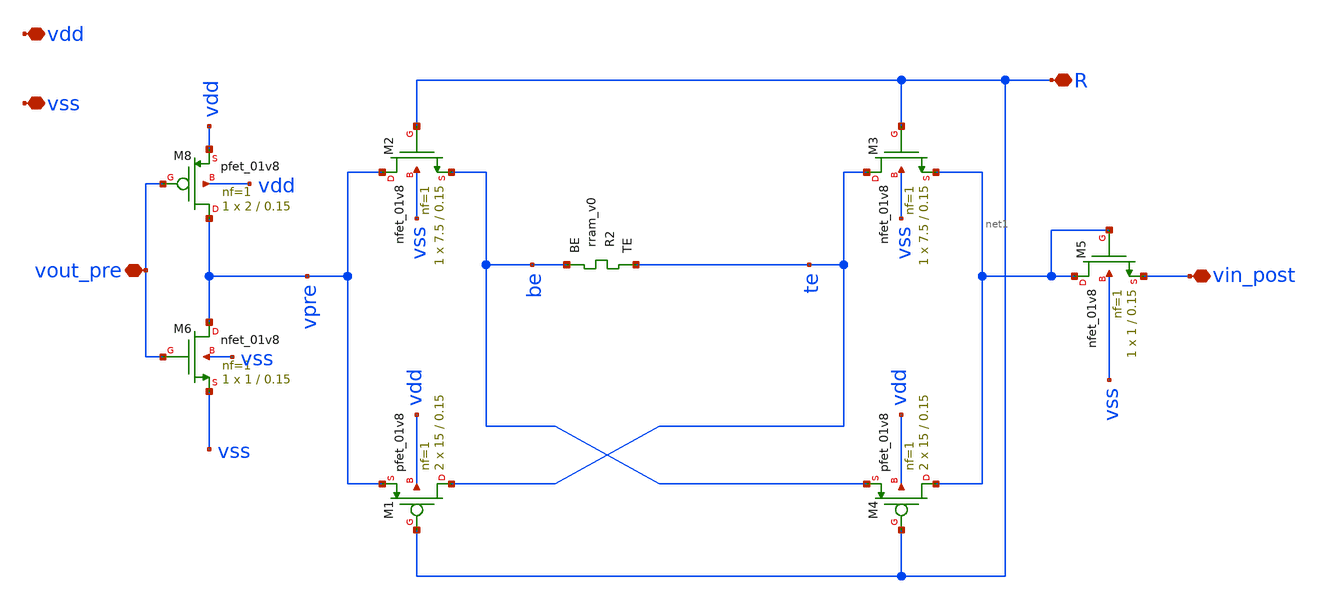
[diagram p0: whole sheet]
** sch_path: Synapse/rstdp_foward.sch
**.subckt rstdp_foward vdd vss R vin_post vout_pre
*.iopin vdd
*.iopin vss
*.iopin R
*.iopin vin_post
*.iopin vout_pre
XR2 te be rram_v0
XM2 vpre R be vss sky130_fd_pr__nfet_01v8 L=0.15 W=7.5 nf=1 ad='int((nf+1)/2) * W/nf * 0.29' as='int((nf+2)/2) * W/nf * 0.29'
+ pd='2*int((nf+1)/2) * (W/nf + 0.29)' ps='2*int((nf+2)/2) * (W/nf + 0.29)' nrd='0.29 / W' nrs='0.29 / W'
+ sa=0 sb=0 sd=0 mult=1 m=1
XM3 te R net1 vss sky130_fd_pr__nfet_01v8 L=0.15 W=7.5 nf=1 ad='int((nf+1)/2) * W/nf * 0.29' as='int((nf+2)/2) * W/nf * 0.29'
+ pd='2*int((nf+1)/2) * (W/nf + 0.29)' ps='2*int((nf+2)/2) * (W/nf + 0.29)' nrd='0.29 / W' nrs='0.29 / W'
+ sa=0 sb=0 sd=0 mult=1 m=1
XM1 te R vpre vdd sky130_fd_pr__pfet_01v8 L=0.15 W=15 nf=1 ad='int((nf+1)/2) * W/nf * 0.29' as='int((nf+2)/2) * W/nf * 0.29'
+ pd='2*int((nf+1)/2) * (W/nf + 0.29)' ps='2*int((nf+2)/2) * (W/nf + 0.29)' nrd='0.29 / W' nrs='0.29 / W'
+ sa=0 sb=0 sd=0 mult=2 m=2
XM4 net1 R be vdd sky130_fd_pr__pfet_01v8 L=0.15 W=15 nf=1 ad='int((nf+1)/2) * W/nf * 0.29' as='int((nf+2)/2) * W/nf * 0.29'
+ pd='2*int((nf+1)/2) * (W/nf + 0.29)' ps='2*int((nf+2)/2) * (W/nf + 0.29)' nrd='0.29 / W' nrs='0.29 / W'
+ sa=0 sb=0 sd=0 mult=2 m=2
XM6 vpre vout_pre vss vss sky130_fd_pr__nfet_01v8 L=0.15 W=1 nf=1 ad='int((1 + 1)/2) * 1 / 1 * 0.29'
+ as='int((1 + 2)/2) * 1 / 1 * 0.29' pd='2*int((1 + 1)/2) * (1 / 1 + 0.29)' ps='2*int((1 + 2)/2) * (1 / 1 + 0.29)'
+ nrd='0.29 / 1 ' nrs='0.29 / 1 ' sa=0 sb=0 sd=0 mult=1 m=1
XM8 vpre vout_pre vdd vdd sky130_fd_pr__pfet_01v8 L=0.15 W=2 nf=1 ad='int((nf+1)/2) * W/nf * 0.29' as='int((nf+2)/2) * W/nf * 0.29'
+ pd='2*int((nf+1)/2) * (W/nf + 0.29)' ps='2*int((nf+2)/2) * (W/nf + 0.29)' nrd='0.29 / W' nrs='0.29 / W'
+ sa=0 sb=0 sd=0 mult=1 m=1
XM5 net1 net1 vin_post vss sky130_fd_pr__nfet_01v8 L=0.15 W=1 nf=1 ad='int((1 + 1)/2) * 1 / 1 * 0.29'
+ as='int((1 + 2)/2) * 1 / 1 * 0.29' pd='2*int((1 + 1)/2) * (1 / 1 + 0.29)' ps='2*int((1 + 2)/2) * (1 / 1 + 0.29)'
+ nrd='0.29 / 1 ' nrs='0.29 / 1 ' sa=0 sb=0 sd=0 mult=1 m=1
**.ends
.end
